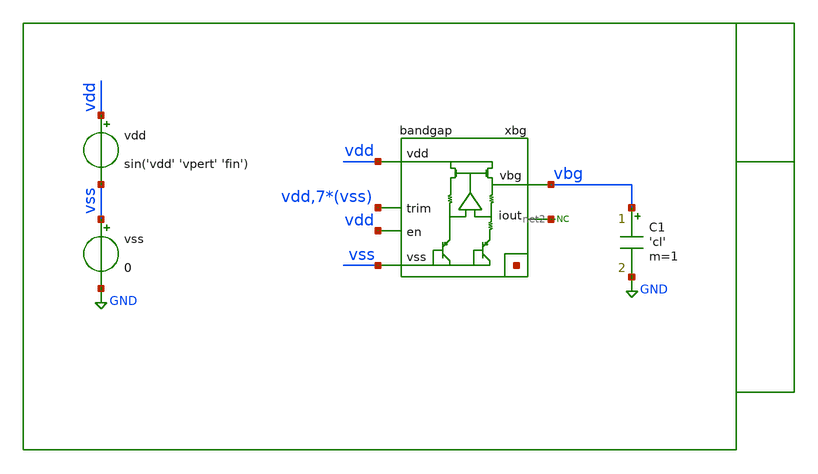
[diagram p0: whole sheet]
** sch_path: xschem/tb/bandgap_cm/bandgap/tr_bandgap_psrr.sch
**.subckt tr_bandgap_psrr
xbg vdd vbg vss net1[7] net1[6] net1[5] net1[4] net1[3] net1[2] net1[1] net1[0] vdd vss vss vss vss
+ vss vss vss net2 vdd bandgap
vss vss GND 0
C1 vbg GND 'cl' m=1
vdd vdd vss sin('vdd' 'vpert' 'fin')
* noconn #net2
**** begin user architecture code

* Control

.param vdd = 3.3
.param cl = 100e-15
.param fin = 1e3
.param vpert = 0.1

.options reltol = 1e-6

.csparam vpert=vpert
.csparam fin=fin

.control

let tmeas = 1/fin
let tsim = 2/fin
let tinit = tsim/1000

save all
tran $&tinit $&tsim

meas tran vbg_min min v(vbg) from=tmeas
meas tran vbg_max max v(vbg) from=tmeas

let psrr = 1/((vbg_max-vbg_min)/vpert)
let psrr_db = vdb(psrr)

print psrr
print psrr_db

.endc
.end


 * Model Corners

.include $::CORNERS/ngspice/tt.spice
*.include $::CORNERS/ngspice/ff.spice
*.include $::CORNERS/ngspice/ss.spice
*.include $::CORNERS/ngspice/sf.spice
*.include $::CORNERS/ngspice/fs.spice

**** end user architecture code
**.ends
.GLOBAL GND
.end
